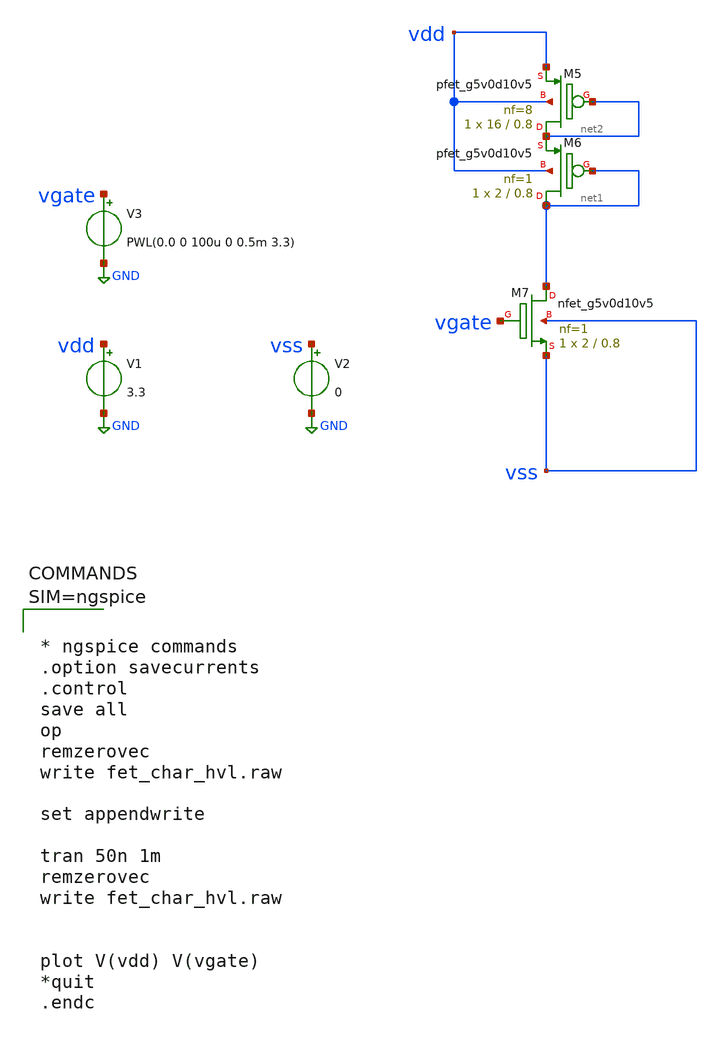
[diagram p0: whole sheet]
** sch_path: xschem/fet_char_hvl.sch
**.subckt fet_char_hvl
V1 vdd GND 3.3
V2 vss GND 0
V3 vgate GND PWL(0.0 0 100u 0 0.5m 3.3)
XM7 net1 vgate vss vss sky130_fd_pr__nfet_g5v0d10v5 L=0.8 W=2 nf=1 ad='int((nf+1)/2) * W/nf * 0.29' as='int((nf+2)/2) * W/nf * 0.29'
+ pd='2*int((nf+1)/2) * (W/nf + 0.29)' ps='2*int((nf+2)/2) * (W/nf + 0.29)' nrd='0.29 / W' nrs='0.29 / W'
+ sa=0 sb=0 sd=0 mult=1 m=1
XM6 net1 net1 net2 vdd sky130_fd_pr__pfet_g5v0d10v5 L=0.8 W=2 nf=1 ad='int((nf+1)/2) * W/nf * 0.29' as='int((nf+2)/2) * W/nf * 0.29'
+ pd='2*int((nf+1)/2) * (W/nf + 0.29)' ps='2*int((nf+2)/2) * (W/nf + 0.29)' nrd='0.29 / W' nrs='0.29 / W'
+ sa=0 sb=0 sd=0 mult=1 m=1
XM5 net2 net2 vdd vdd sky130_fd_pr__pfet_g5v0d10v5 L=0.8 W=16 nf=8 ad='int((nf+1)/2) * W/nf * 0.29' as='int((nf+2)/2) * W/nf * 0.29'
+ pd='2*int((nf+1)/2) * (W/nf + 0.29)' ps='2*int((nf+2)/2) * (W/nf + 0.29)' nrd='0.29 / W' nrs='0.29 / W'
+ sa=0 sb=0 sd=0 mult=1 m=1
**** begin user architecture code

** opencircuitdesign pdks install
.lib $::SKYWATER_MODELS/sky130.lib.spice tt
.include $::SKYWATER_STDCELLS/sky130_fd_sc_hd.spice
.temp 27




* ngspice commands
.option savecurrents
.control
save all
op
remzerovec
write fet_char_hvl.raw

set appendwrite

tran 50n 1m
remzerovec
write fet_char_hvl.raw


plot V(vdd) V(vgate)
*quit
.endc



**** end user architecture code
**.ends
.GLOBAL GND
.end
